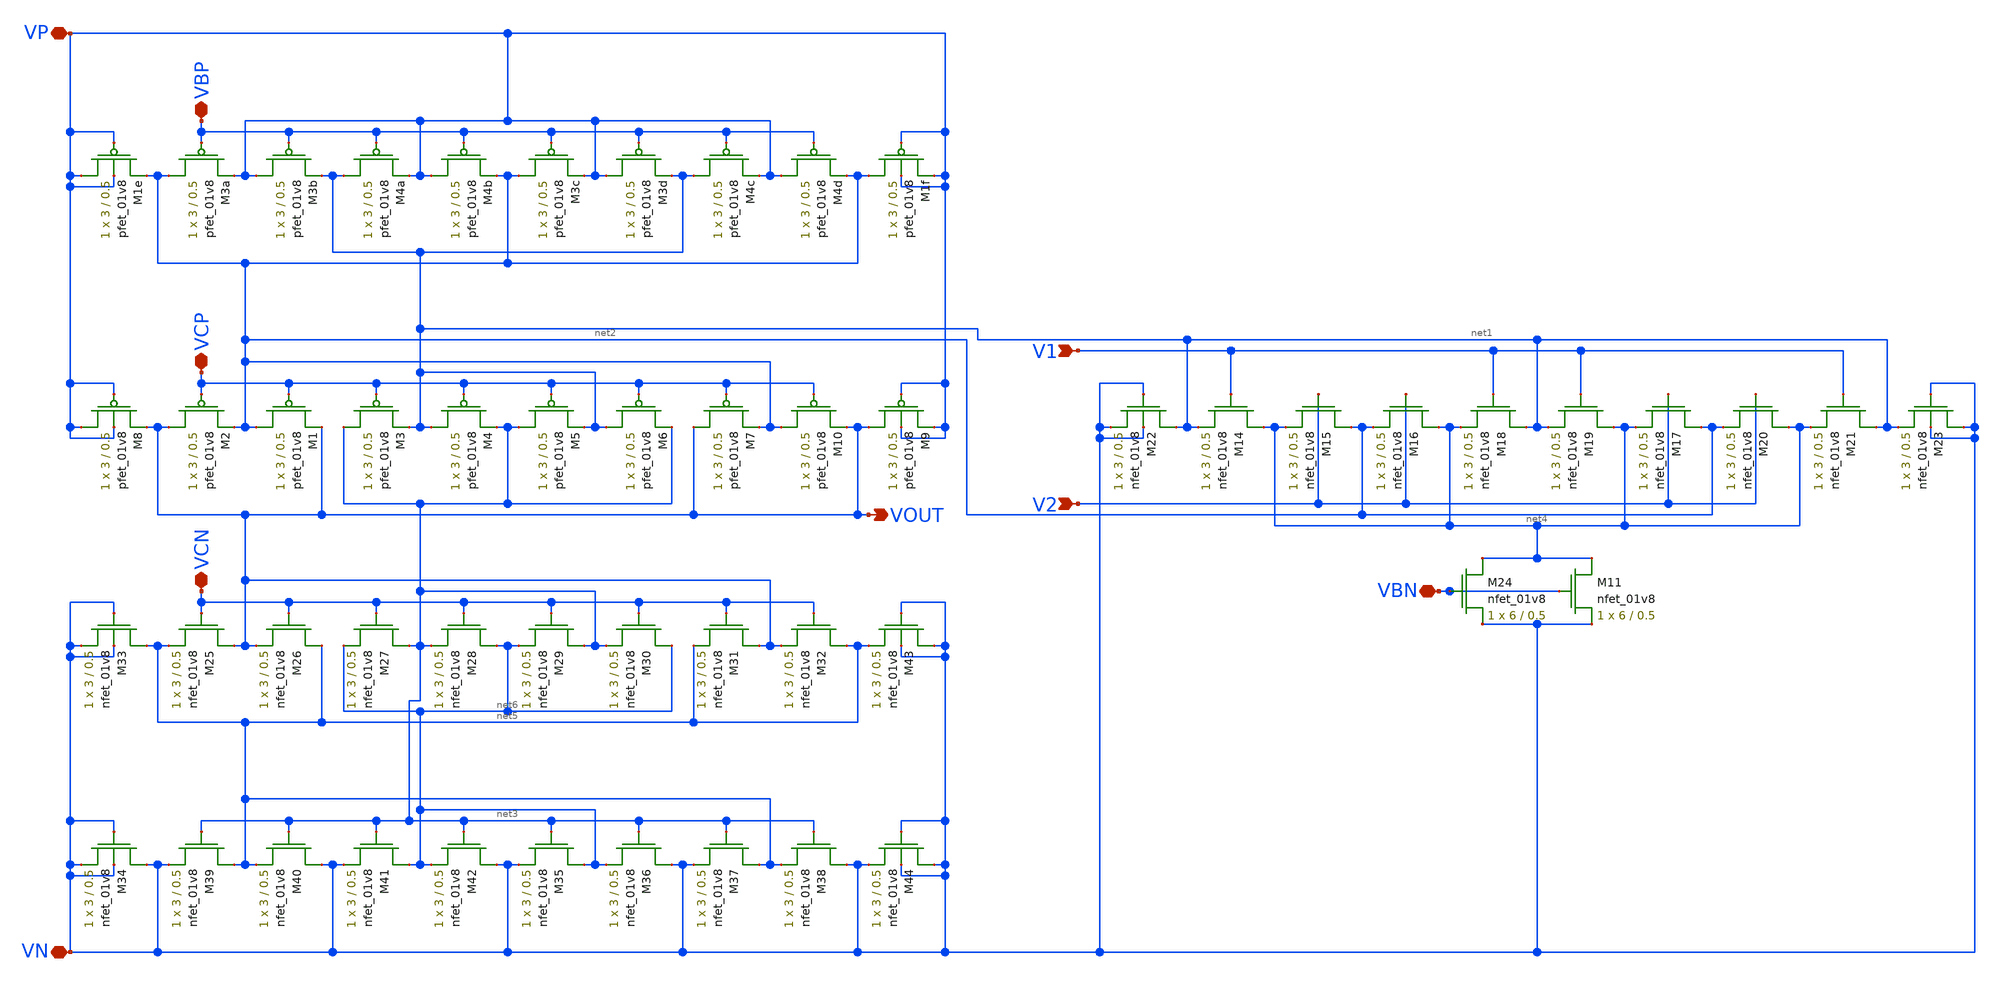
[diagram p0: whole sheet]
** sch_path: mp3/schematics/folded_cascode_differential_amplifier.sch
**.subckt folded_cascode_differential_amplifier VBP VCP V1 V2 VBN VCN VP VN VOUT
*.iopin VBP
*.iopin VCP
*.ipin V1
*.ipin V2
*.iopin VBN
*.iopin VCN
*.iopin VP
*.iopin VN
*.opin VOUT
XM3b VP VBP net1 VDD sky130_fd_pr__pfet_01v8 L=0.5 W=3 nf=1 ad='int((nf+1)/2) * W/nf * 0.29' as='int((nf+2)/2) * W/nf * 0.29'
+ pd='2*int((nf+1)/2) * (W/nf + 0.29)' ps='2*int((nf+2)/2) * (W/nf + 0.29)' nrd='0.29 / W' nrs='0.29 / W'
+ sa=0 sb=0 sd=0 mult=1 m=1
XM3a net2 VBP VP VDD sky130_fd_pr__pfet_01v8 L=0.5 W=3 nf=1 ad='int((nf+1)/2) * W/nf * 0.29' as='int((nf+2)/2) * W/nf * 0.29'
+ pd='2*int((nf+1)/2) * (W/nf + 0.29)' ps='2*int((nf+2)/2) * (W/nf + 0.29)' nrd='0.29 / W' nrs='0.29 / W'
+ sa=0 sb=0 sd=0 mult=1 m=1
XM4a net1 VBP VP VDD sky130_fd_pr__pfet_01v8 L=0.5 W=3 nf=1 ad='int((nf+1)/2) * W/nf * 0.29' as='int((nf+2)/2) * W/nf * 0.29'
+ pd='2*int((nf+1)/2) * (W/nf + 0.29)' ps='2*int((nf+2)/2) * (W/nf + 0.29)' nrd='0.29 / W' nrs='0.29 / W'
+ sa=0 sb=0 sd=0 mult=1 m=1
XM4b VP VBP net2 VDD sky130_fd_pr__pfet_01v8 L=0.5 W=3 nf=1 ad='int((nf+1)/2) * W/nf * 0.29' as='int((nf+2)/2) * W/nf * 0.29'
+ pd='2*int((nf+1)/2) * (W/nf + 0.29)' ps='2*int((nf+2)/2) * (W/nf + 0.29)' nrd='0.29 / W' nrs='0.29 / W'
+ sa=0 sb=0 sd=0 mult=1 m=1
XM3c net2 VBP VP VDD sky130_fd_pr__pfet_01v8 L=0.5 W=3 nf=1 ad='int((nf+1)/2) * W/nf * 0.29' as='int((nf+2)/2) * W/nf * 0.29'
+ pd='2*int((nf+1)/2) * (W/nf + 0.29)' ps='2*int((nf+2)/2) * (W/nf + 0.29)' nrd='0.29 / W' nrs='0.29 / W'
+ sa=0 sb=0 sd=0 mult=1 m=1
XM3d VP VBP net1 VDD sky130_fd_pr__pfet_01v8 L=0.5 W=3 nf=1 ad='int((nf+1)/2) * W/nf * 0.29' as='int((nf+2)/2) * W/nf * 0.29'
+ pd='2*int((nf+1)/2) * (W/nf + 0.29)' ps='2*int((nf+2)/2) * (W/nf + 0.29)' nrd='0.29 / W' nrs='0.29 / W'
+ sa=0 sb=0 sd=0 mult=1 m=1
XM4c net1 VBP VP VDD sky130_fd_pr__pfet_01v8 L=0.5 W=3 nf=1 ad='int((nf+1)/2) * W/nf * 0.29' as='int((nf+2)/2) * W/nf * 0.29'
+ pd='2*int((nf+1)/2) * (W/nf + 0.29)' ps='2*int((nf+2)/2) * (W/nf + 0.29)' nrd='0.29 / W' nrs='0.29 / W'
+ sa=0 sb=0 sd=0 mult=1 m=1
XM1e VP VP net2 VP sky130_fd_pr__pfet_01v8 L=0.5 W=3 nf=1 ad='int((nf+1)/2) * W/nf * 0.29' as='int((nf+2)/2) * W/nf * 0.29'
+ pd='2*int((nf+1)/2) * (W/nf + 0.29)' ps='2*int((nf+2)/2) * (W/nf + 0.29)' nrd='0.29 / W' nrs='0.29 / W'
+ sa=0 sb=0 sd=0 mult=1 m=1
XM1f net2 VP VP VP sky130_fd_pr__pfet_01v8 L=0.5 W=3 nf=1 ad='int((nf+1)/2) * W/nf * 0.29' as='int((nf+2)/2) * W/nf * 0.29'
+ pd='2*int((nf+1)/2) * (W/nf + 0.29)' ps='2*int((nf+2)/2) * (W/nf + 0.29)' nrd='0.29 / W' nrs='0.29 / W'
+ sa=0 sb=0 sd=0 mult=1 m=1
XM4d VP VBP net2 VDD sky130_fd_pr__pfet_01v8 L=0.5 W=3 nf=1 ad='int((nf+1)/2) * W/nf * 0.29' as='int((nf+2)/2) * W/nf * 0.29'
+ pd='2*int((nf+1)/2) * (W/nf + 0.29)' ps='2*int((nf+2)/2) * (W/nf + 0.29)' nrd='0.29 / W' nrs='0.29 / W'
+ sa=0 sb=0 sd=0 mult=1 m=1
XM1 net2 VCP VOUT VDD sky130_fd_pr__pfet_01v8 L=0.5 W=3 nf=1 ad='int((nf+1)/2) * W/nf * 0.29' as='int((nf+2)/2) * W/nf * 0.29'
+ pd='2*int((nf+1)/2) * (W/nf + 0.29)' ps='2*int((nf+2)/2) * (W/nf + 0.29)' nrd='0.29 / W' nrs='0.29 / W'
+ sa=0 sb=0 sd=0 mult=1 m=1
XM2 VOUT VCP net2 VDD sky130_fd_pr__pfet_01v8 L=0.5 W=3 nf=1 ad='int((nf+1)/2) * W/nf * 0.29' as='int((nf+2)/2) * W/nf * 0.29'
+ pd='2*int((nf+1)/2) * (W/nf + 0.29)' ps='2*int((nf+2)/2) * (W/nf + 0.29)' nrd='0.29 / W' nrs='0.29 / W'
+ sa=0 sb=0 sd=0 mult=1 m=1
XM3 net3 VCP net1 VDD sky130_fd_pr__pfet_01v8 L=0.5 W=3 nf=1 ad='int((nf+1)/2) * W/nf * 0.29' as='int((nf+2)/2) * W/nf * 0.29'
+ pd='2*int((nf+1)/2) * (W/nf + 0.29)' ps='2*int((nf+2)/2) * (W/nf + 0.29)' nrd='0.29 / W' nrs='0.29 / W'
+ sa=0 sb=0 sd=0 mult=1 m=1
XM4 net1 VCP net3 VDD sky130_fd_pr__pfet_01v8 L=0.5 W=3 nf=1 ad='int((nf+1)/2) * W/nf * 0.29' as='int((nf+2)/2) * W/nf * 0.29'
+ pd='2*int((nf+1)/2) * (W/nf + 0.29)' ps='2*int((nf+2)/2) * (W/nf + 0.29)' nrd='0.29 / W' nrs='0.29 / W'
+ sa=0 sb=0 sd=0 mult=1 m=1
XM5 net3 VCP net1 VDD sky130_fd_pr__pfet_01v8 L=0.5 W=3 nf=1 ad='int((nf+1)/2) * W/nf * 0.29' as='int((nf+2)/2) * W/nf * 0.29'
+ pd='2*int((nf+1)/2) * (W/nf + 0.29)' ps='2*int((nf+2)/2) * (W/nf + 0.29)' nrd='0.29 / W' nrs='0.29 / W'
+ sa=0 sb=0 sd=0 mult=1 m=1
XM6 net1 VCP net3 VDD sky130_fd_pr__pfet_01v8 L=0.5 W=3 nf=1 ad='int((nf+1)/2) * W/nf * 0.29' as='int((nf+2)/2) * W/nf * 0.29'
+ pd='2*int((nf+1)/2) * (W/nf + 0.29)' ps='2*int((nf+2)/2) * (W/nf + 0.29)' nrd='0.29 / W' nrs='0.29 / W'
+ sa=0 sb=0 sd=0 mult=1 m=1
XM7 VOUT VCP net2 VDD sky130_fd_pr__pfet_01v8 L=0.5 W=3 nf=1 ad='int((nf+1)/2) * W/nf * 0.29' as='int((nf+2)/2) * W/nf * 0.29'
+ pd='2*int((nf+1)/2) * (W/nf + 0.29)' ps='2*int((nf+2)/2) * (W/nf + 0.29)' nrd='0.29 / W' nrs='0.29 / W'
+ sa=0 sb=0 sd=0 mult=1 m=1
XM8 VP VP VOUT VP sky130_fd_pr__pfet_01v8 L=0.5 W=3 nf=1 ad='int((nf+1)/2) * W/nf * 0.29' as='int((nf+2)/2) * W/nf * 0.29'
+ pd='2*int((nf+1)/2) * (W/nf + 0.29)' ps='2*int((nf+2)/2) * (W/nf + 0.29)' nrd='0.29 / W' nrs='0.29 / W'
+ sa=0 sb=0 sd=0 mult=1 m=1
XM9 VOUT VP VP VP sky130_fd_pr__pfet_01v8 L=0.5 W=3 nf=1 ad='int((nf+1)/2) * W/nf * 0.29' as='int((nf+2)/2) * W/nf * 0.29'
+ pd='2*int((nf+1)/2) * (W/nf + 0.29)' ps='2*int((nf+2)/2) * (W/nf + 0.29)' nrd='0.29 / W' nrs='0.29 / W'
+ sa=0 sb=0 sd=0 mult=1 m=1
XM10 net2 VCP VOUT VDD sky130_fd_pr__pfet_01v8 L=0.5 W=3 nf=1 ad='int((nf+1)/2) * W/nf * 0.29' as='int((nf+2)/2) * W/nf * 0.29'
+ pd='2*int((nf+1)/2) * (W/nf + 0.29)' ps='2*int((nf+2)/2) * (W/nf + 0.29)' nrd='0.29 / W' nrs='0.29 / W'
+ sa=0 sb=0 sd=0 mult=1 m=1
XM14 net4 V1 net1 GND sky130_fd_pr__nfet_01v8 L=0.5 W=3 nf=1 ad='int((nf+1)/2) * W/nf * 0.29' as='int((nf+2)/2) * W/nf * 0.29'
+ pd='2*int((nf+1)/2) * (W/nf + 0.29)' ps='2*int((nf+2)/2) * (W/nf + 0.29)' nrd='0.29 / W' nrs='0.29 / W'
+ sa=0 sb=0 sd=0 mult=1 m=1
XM22 net1 VN VN VN sky130_fd_pr__nfet_01v8 L=0.5 W=3 nf=1 ad='int((nf+1)/2) * W/nf * 0.29' as='int((nf+2)/2) * W/nf * 0.29'
+ pd='2*int((nf+1)/2) * (W/nf + 0.29)' ps='2*int((nf+2)/2) * (W/nf + 0.29)' nrd='0.29 / W' nrs='0.29 / W'
+ sa=0 sb=0 sd=0 mult=1 m=1
XM23 VN VN net1 VN sky130_fd_pr__nfet_01v8 L=0.5 W=3 nf=1 ad='int((nf+1)/2) * W/nf * 0.29' as='int((nf+2)/2) * W/nf * 0.29'
+ pd='2*int((nf+1)/2) * (W/nf + 0.29)' ps='2*int((nf+2)/2) * (W/nf + 0.29)' nrd='0.29 / W' nrs='0.29 / W'
+ sa=0 sb=0 sd=0 mult=1 m=1
XM15 net2 V2 net4 GND sky130_fd_pr__nfet_01v8 L=0.5 W=3 nf=1 ad='int((nf+1)/2) * W/nf * 0.29' as='int((nf+2)/2) * W/nf * 0.29'
+ pd='2*int((nf+1)/2) * (W/nf + 0.29)' ps='2*int((nf+2)/2) * (W/nf + 0.29)' nrd='0.29 / W' nrs='0.29 / W'
+ sa=0 sb=0 sd=0 mult=1 m=1
XM16 net4 V2 net2 GND sky130_fd_pr__nfet_01v8 L=0.5 W=3 nf=1 ad='int((nf+1)/2) * W/nf * 0.29' as='int((nf+2)/2) * W/nf * 0.29'
+ pd='2*int((nf+1)/2) * (W/nf + 0.29)' ps='2*int((nf+2)/2) * (W/nf + 0.29)' nrd='0.29 / W' nrs='0.29 / W'
+ sa=0 sb=0 sd=0 mult=1 m=1
XM17 net2 V2 net4 GND sky130_fd_pr__nfet_01v8 L=0.5 W=3 nf=1 ad='int((nf+1)/2) * W/nf * 0.29' as='int((nf+2)/2) * W/nf * 0.29'
+ pd='2*int((nf+1)/2) * (W/nf + 0.29)' ps='2*int((nf+2)/2) * (W/nf + 0.29)' nrd='0.29 / W' nrs='0.29 / W'
+ sa=0 sb=0 sd=0 mult=1 m=1
XM18 net1 V1 net4 GND sky130_fd_pr__nfet_01v8 L=0.5 W=3 nf=1 ad='int((nf+1)/2) * W/nf * 0.29' as='int((nf+2)/2) * W/nf * 0.29'
+ pd='2*int((nf+1)/2) * (W/nf + 0.29)' ps='2*int((nf+2)/2) * (W/nf + 0.29)' nrd='0.29 / W' nrs='0.29 / W'
+ sa=0 sb=0 sd=0 mult=1 m=1
XM19 net4 V1 net1 GND sky130_fd_pr__nfet_01v8 L=0.5 W=3 nf=1 ad='int((nf+1)/2) * W/nf * 0.29' as='int((nf+2)/2) * W/nf * 0.29'
+ pd='2*int((nf+1)/2) * (W/nf + 0.29)' ps='2*int((nf+2)/2) * (W/nf + 0.29)' nrd='0.29 / W' nrs='0.29 / W'
+ sa=0 sb=0 sd=0 mult=1 m=1
XM20 net4 V2 net2 GND sky130_fd_pr__nfet_01v8 L=0.5 W=3 nf=1 ad='int((nf+1)/2) * W/nf * 0.29' as='int((nf+2)/2) * W/nf * 0.29'
+ pd='2*int((nf+1)/2) * (W/nf + 0.29)' ps='2*int((nf+2)/2) * (W/nf + 0.29)' nrd='0.29 / W' nrs='0.29 / W'
+ sa=0 sb=0 sd=0 mult=1 m=1
XM21 net1 V1 net4 GND sky130_fd_pr__nfet_01v8 L=0.5 W=3 nf=1 ad='int((nf+1)/2) * W/nf * 0.29' as='int((nf+2)/2) * W/nf * 0.29'
+ pd='2*int((nf+1)/2) * (W/nf + 0.29)' ps='2*int((nf+2)/2) * (W/nf + 0.29)' nrd='0.29 / W' nrs='0.29 / W'
+ sa=0 sb=0 sd=0 mult=1 m=1
XM24 net4 VBN VN GND sky130_fd_pr__nfet_01v8 L=0.5 W=6 nf=1 ad='int((nf+1)/2) * W/nf * 0.29' as='int((nf+2)/2) * W/nf * 0.29'
+ pd='2*int((nf+1)/2) * (W/nf + 0.29)' ps='2*int((nf+2)/2) * (W/nf + 0.29)' nrd='0.29 / W' nrs='0.29 / W'
+ sa=0 sb=0 sd=0 mult=1 m=1
XM29 net3 VCN net6 GND sky130_fd_pr__nfet_01v8 L=0.5 W=3 nf=1 ad='int((nf+1)/2) * W/nf * 0.29' as='int((nf+2)/2) * W/nf * 0.29'
+ pd='2*int((nf+1)/2) * (W/nf + 0.29)' ps='2*int((nf+2)/2) * (W/nf + 0.29)' nrd='0.29 / W' nrs='0.29 / W'
+ sa=0 sb=0 sd=0 mult=1 m=1
XM30 net6 VCN net3 GND sky130_fd_pr__nfet_01v8 L=0.5 W=3 nf=1 ad='int((nf+1)/2) * W/nf * 0.29' as='int((nf+2)/2) * W/nf * 0.29'
+ pd='2*int((nf+1)/2) * (W/nf + 0.29)' ps='2*int((nf+2)/2) * (W/nf + 0.29)' nrd='0.29 / W' nrs='0.29 / W'
+ sa=0 sb=0 sd=0 mult=1 m=1
XM31 VOUT VCN net5 GND sky130_fd_pr__nfet_01v8 L=0.5 W=3 nf=1 ad='int((nf+1)/2) * W/nf * 0.29' as='int((nf+2)/2) * W/nf * 0.29'
+ pd='2*int((nf+1)/2) * (W/nf + 0.29)' ps='2*int((nf+2)/2) * (W/nf + 0.29)' nrd='0.29 / W' nrs='0.29 / W'
+ sa=0 sb=0 sd=0 mult=1 m=1
XM32 net5 VCN VOUT GND sky130_fd_pr__nfet_01v8 L=0.5 W=3 nf=1 ad='int((nf+1)/2) * W/nf * 0.29' as='int((nf+2)/2) * W/nf * 0.29'
+ pd='2*int((nf+1)/2) * (W/nf + 0.29)' ps='2*int((nf+2)/2) * (W/nf + 0.29)' nrd='0.29 / W' nrs='0.29 / W'
+ sa=0 sb=0 sd=0 mult=1 m=1
XM25 VOUT VCN net5 GND sky130_fd_pr__nfet_01v8 L=0.5 W=3 nf=1 ad='int((nf+1)/2) * W/nf * 0.29' as='int((nf+2)/2) * W/nf * 0.29'
+ pd='2*int((nf+1)/2) * (W/nf + 0.29)' ps='2*int((nf+2)/2) * (W/nf + 0.29)' nrd='0.29 / W' nrs='0.29 / W'
+ sa=0 sb=0 sd=0 mult=1 m=1
XM26 net5 VCN VOUT GND sky130_fd_pr__nfet_01v8 L=0.5 W=3 nf=1 ad='int((nf+1)/2) * W/nf * 0.29' as='int((nf+2)/2) * W/nf * 0.29'
+ pd='2*int((nf+1)/2) * (W/nf + 0.29)' ps='2*int((nf+2)/2) * (W/nf + 0.29)' nrd='0.29 / W' nrs='0.29 / W'
+ sa=0 sb=0 sd=0 mult=1 m=1
XM27 net3 VCN net6 GND sky130_fd_pr__nfet_01v8 L=0.5 W=3 nf=1 ad='int((nf+1)/2) * W/nf * 0.29' as='int((nf+2)/2) * W/nf * 0.29'
+ pd='2*int((nf+1)/2) * (W/nf + 0.29)' ps='2*int((nf+2)/2) * (W/nf + 0.29)' nrd='0.29 / W' nrs='0.29 / W'
+ sa=0 sb=0 sd=0 mult=1 m=1
XM28 net6 VCN net3 GND sky130_fd_pr__nfet_01v8 L=0.5 W=3 nf=1 ad='int((nf+1)/2) * W/nf * 0.29' as='int((nf+2)/2) * W/nf * 0.29'
+ pd='2*int((nf+1)/2) * (W/nf + 0.29)' ps='2*int((nf+2)/2) * (W/nf + 0.29)' nrd='0.29 / W' nrs='0.29 / W'
+ sa=0 sb=0 sd=0 mult=1 m=1
XM35 net6 net3 VN GND sky130_fd_pr__nfet_01v8 L=0.5 W=3 nf=1 ad='int((nf+1)/2) * W/nf * 0.29' as='int((nf+2)/2) * W/nf * 0.29'
+ pd='2*int((nf+1)/2) * (W/nf + 0.29)' ps='2*int((nf+2)/2) * (W/nf + 0.29)' nrd='0.29 / W' nrs='0.29 / W'
+ sa=0 sb=0 sd=0 mult=1 m=1
XM36 VN net3 net6 GND sky130_fd_pr__nfet_01v8 L=0.5 W=3 nf=1 ad='int((nf+1)/2) * W/nf * 0.29' as='int((nf+2)/2) * W/nf * 0.29'
+ pd='2*int((nf+1)/2) * (W/nf + 0.29)' ps='2*int((nf+2)/2) * (W/nf + 0.29)' nrd='0.29 / W' nrs='0.29 / W'
+ sa=0 sb=0 sd=0 mult=1 m=1
XM37 net5 net3 VN GND sky130_fd_pr__nfet_01v8 L=0.5 W=3 nf=1 ad='int((nf+1)/2) * W/nf * 0.29' as='int((nf+2)/2) * W/nf * 0.29'
+ pd='2*int((nf+1)/2) * (W/nf + 0.29)' ps='2*int((nf+2)/2) * (W/nf + 0.29)' nrd='0.29 / W' nrs='0.29 / W'
+ sa=0 sb=0 sd=0 mult=1 m=1
XM38 VN net3 net5 GND sky130_fd_pr__nfet_01v8 L=0.5 W=3 nf=1 ad='int((nf+1)/2) * W/nf * 0.29' as='int((nf+2)/2) * W/nf * 0.29'
+ pd='2*int((nf+1)/2) * (W/nf + 0.29)' ps='2*int((nf+2)/2) * (W/nf + 0.29)' nrd='0.29 / W' nrs='0.29 / W'
+ sa=0 sb=0 sd=0 mult=1 m=1
XM39 net5 net3 VN GND sky130_fd_pr__nfet_01v8 L=0.5 W=3 nf=1 ad='int((nf+1)/2) * W/nf * 0.29' as='int((nf+2)/2) * W/nf * 0.29'
+ pd='2*int((nf+1)/2) * (W/nf + 0.29)' ps='2*int((nf+2)/2) * (W/nf + 0.29)' nrd='0.29 / W' nrs='0.29 / W'
+ sa=0 sb=0 sd=0 mult=1 m=1
XM40 VN net3 net5 GND sky130_fd_pr__nfet_01v8 L=0.5 W=3 nf=1 ad='int((nf+1)/2) * W/nf * 0.29' as='int((nf+2)/2) * W/nf * 0.29'
+ pd='2*int((nf+1)/2) * (W/nf + 0.29)' ps='2*int((nf+2)/2) * (W/nf + 0.29)' nrd='0.29 / W' nrs='0.29 / W'
+ sa=0 sb=0 sd=0 mult=1 m=1
XM41 net6 net3 VN GND sky130_fd_pr__nfet_01v8 L=0.5 W=3 nf=1 ad='int((nf+1)/2) * W/nf * 0.29' as='int((nf+2)/2) * W/nf * 0.29'
+ pd='2*int((nf+1)/2) * (W/nf + 0.29)' ps='2*int((nf+2)/2) * (W/nf + 0.29)' nrd='0.29 / W' nrs='0.29 / W'
+ sa=0 sb=0 sd=0 mult=1 m=1
XM42 VN net3 net6 GND sky130_fd_pr__nfet_01v8 L=0.5 W=3 nf=1 ad='int((nf+1)/2) * W/nf * 0.29' as='int((nf+2)/2) * W/nf * 0.29'
+ pd='2*int((nf+1)/2) * (W/nf + 0.29)' ps='2*int((nf+2)/2) * (W/nf + 0.29)' nrd='0.29 / W' nrs='0.29 / W'
+ sa=0 sb=0 sd=0 mult=1 m=1
XM33 net5 VN VN VN sky130_fd_pr__nfet_01v8 L=0.5 W=3 nf=1 ad='int((nf+1)/2) * W/nf * 0.29' as='int((nf+2)/2) * W/nf * 0.29'
+ pd='2*int((nf+1)/2) * (W/nf + 0.29)' ps='2*int((nf+2)/2) * (W/nf + 0.29)' nrd='0.29 / W' nrs='0.29 / W'
+ sa=0 sb=0 sd=0 mult=1 m=1
XM34 VN VN VN VN sky130_fd_pr__nfet_01v8 L=0.5 W=3 nf=1 ad='int((nf+1)/2) * W/nf * 0.29' as='int((nf+2)/2) * W/nf * 0.29'
+ pd='2*int((nf+1)/2) * (W/nf + 0.29)' ps='2*int((nf+2)/2) * (W/nf + 0.29)' nrd='0.29 / W' nrs='0.29 / W'
+ sa=0 sb=0 sd=0 mult=1 m=1
XM43 VN VN net5 VN sky130_fd_pr__nfet_01v8 L=0.5 W=3 nf=1 ad='int((nf+1)/2) * W/nf * 0.29' as='int((nf+2)/2) * W/nf * 0.29'
+ pd='2*int((nf+1)/2) * (W/nf + 0.29)' ps='2*int((nf+2)/2) * (W/nf + 0.29)' nrd='0.29 / W' nrs='0.29 / W'
+ sa=0 sb=0 sd=0 mult=1 m=1
XM44 VN VN VN VN sky130_fd_pr__nfet_01v8 L=0.5 W=3 nf=1 ad='int((nf+1)/2) * W/nf * 0.29' as='int((nf+2)/2) * W/nf * 0.29'
+ pd='2*int((nf+1)/2) * (W/nf + 0.29)' ps='2*int((nf+2)/2) * (W/nf + 0.29)' nrd='0.29 / W' nrs='0.29 / W'
+ sa=0 sb=0 sd=0 mult=1 m=1
XM11 net4 VBN VN GND sky130_fd_pr__nfet_01v8 L=0.5 W=6 nf=1 ad='int((nf+1)/2) * W/nf * 0.29' as='int((nf+2)/2) * W/nf * 0.29'
+ pd='2*int((nf+1)/2) * (W/nf + 0.29)' ps='2*int((nf+2)/2) * (W/nf + 0.29)' nrd='0.29 / W' nrs='0.29 / W'
+ sa=0 sb=0 sd=0 mult=1 m=1
**.ends
.end
